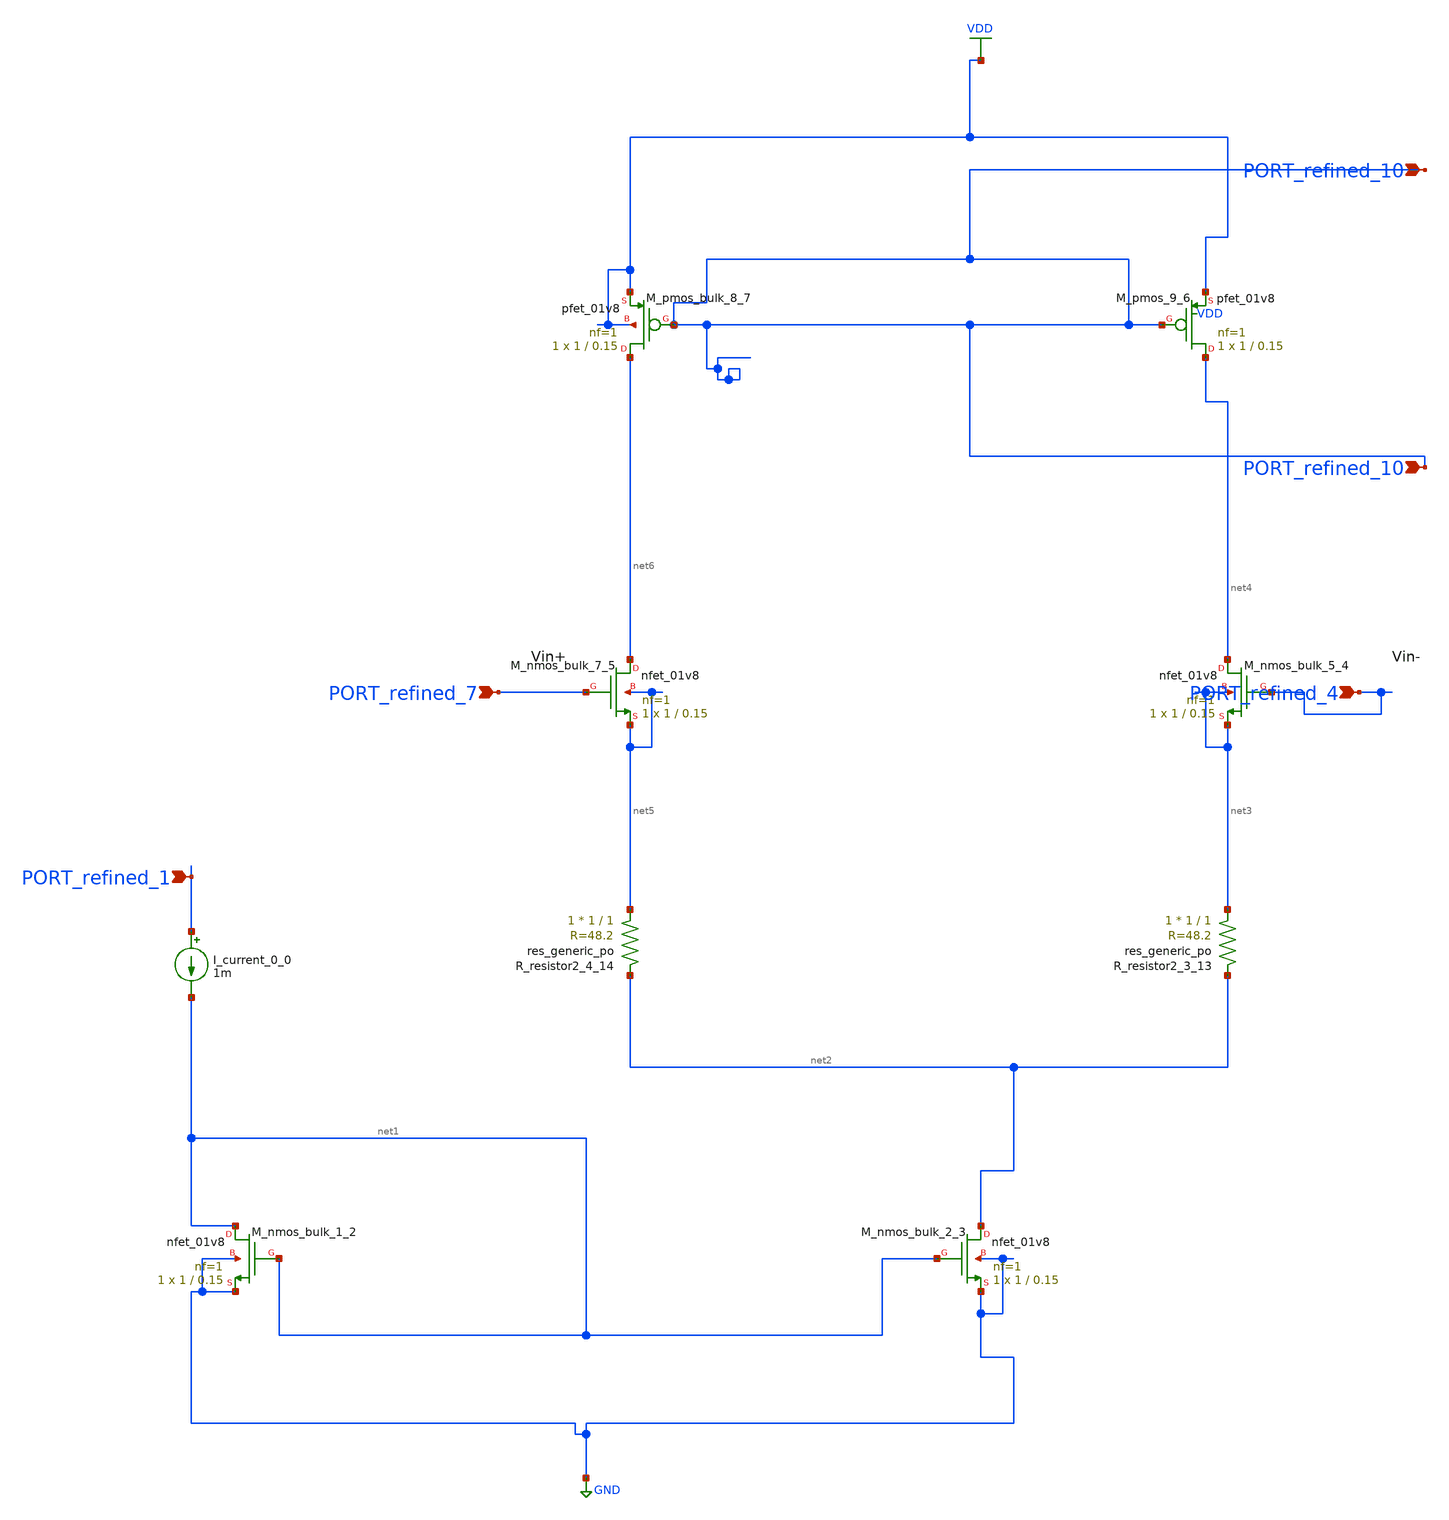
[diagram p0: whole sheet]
** sch_path: schematics/10_1007_s42452-022-05100-1_05_001_crop1.sch
**.subckt 10_1007_s42452-022-05100-1_05_001_crop1 PORT_refined_10 PORT_refined_10 PORT_refined_1
*+ PORT_refined_7 PORT_refined_4
*.ipin PORT_refined_10
*.ipin PORT_refined_10
*.ipin PORT_refined_1
*.ipin PORT_refined_7
*.ipin PORT_refined_4
I_current_0_0 PORT_refined_1 net1 1m
XM_nmos_bulk_1_2 net1 net1 GND GND sky130_fd_pr__nfet_01v8 L=0.15 W=1 nf=1 ad='int((1 + 1)/2) * 1 / 1 * 0.29'
+ as='int((1 + 2)/2) * 1 / 1 * 0.29' pd='2*int((1 + 1)/2) * (1 / 1 + 0.29)' ps='2*int((1 + 2)/2) * (1 / 1 + 0.29)'
+ nrd='0.29 / 1 ' nrs='0.29 / 1 ' sa=0 sb=0 sd=0 mult=1 m=1
XM_nmos_bulk_2_3 net2 net1 GND GND sky130_fd_pr__nfet_01v8 L=0.15 W=1 nf=1 ad='int((1 + 1)/2) * 1 / 1 * 0.29'
+ as='int((1 + 2)/2) * 1 / 1 * 0.29' pd='2*int((1 + 1)/2) * (1 / 1 + 0.29)' ps='2*int((1 + 2)/2) * (1 / 1 + 0.29)'
+ nrd='0.29 / 1 ' nrs='0.29 / 1 ' sa=0 sb=0 sd=0 mult=1 m=1
XM_nmos_bulk_5_4 net4 PORT_refined_4 net3 net3 sky130_fd_pr__nfet_01v8 L=0.15 W=1 nf=1 ad='int((1 + 1)/2) * 1 / 1 * 0.29'
+ as='int((1 + 2)/2) * 1 / 1 * 0.29' pd='2*int((1 + 1)/2) * (1 / 1 + 0.29)' ps='2*int((1 + 2)/2) * (1 / 1 + 0.29)'
+ nrd='0.29 / 1 ' nrs='0.29 / 1 ' sa=0 sb=0 sd=0 mult=1 m=1
XM_nmos_bulk_7_5 net6 PORT_refined_7 net5 net5 sky130_fd_pr__nfet_01v8 L=0.15 W=1 nf=1 ad='int((1 + 1)/2) * 1 / 1 * 0.29'
+ as='int((1 + 2)/2) * 1 / 1 * 0.29' pd='2*int((1 + 1)/2) * (1 / 1 + 0.29)' ps='2*int((1 + 2)/2) * (1 / 1 + 0.29)'
+ nrd='0.29 / 1 ' nrs='0.29 / 1 ' sa=0 sb=0 sd=0 mult=1 m=1
XM_pmos_9_6 net4 PORT_refined_10 VDD VDD sky130_fd_pr__pfet_01v8 L=0.15 W=1 nf=1 ad='int((1 + 1)/2) * 1 / 1 * 0.29'
+ as='int((1 + 2)/2) * 1 / 1 * 0.29' pd='2*int((1 + 1)/2) * (1 / 1 + 0.29)' ps='2*int((1 + 2)/2) * (1 / 1 + 0.29)'
+ nrd='0.29 / 1 ' nrs='0.29 / 1 ' sa=0 sb=0 sd=0 mult=1 m=1
XM_pmos_bulk_8_7 net6 PORT_refined_10 VDD VDD sky130_fd_pr__pfet_01v8 L=0.15 W=1 nf=1 ad='int((1 + 1)/2) * 1 / 1 * 0.29'
+ as='int((1 + 2)/2) * 1 / 1 * 0.29' pd='2*int((1 + 1)/2) * (1 / 1 + 0.29)' ps='2*int((1 + 2)/2) * (1 / 1 + 0.29)'
+ nrd='0.29 / 1 ' nrs='0.29 / 1 ' sa=0 sb=0 sd=0 mult=1 m=1
XR_resistor2_3_13 net3 net2 sky130_fd_pr__res_generic_po W=1 L=1 m=1
XR_resistor2_4_14 net5 net2 sky130_fd_pr__res_generic_po W=1 L=1 m=1
**.ends
.GLOBAL GND
.GLOBAL VDD
.end
